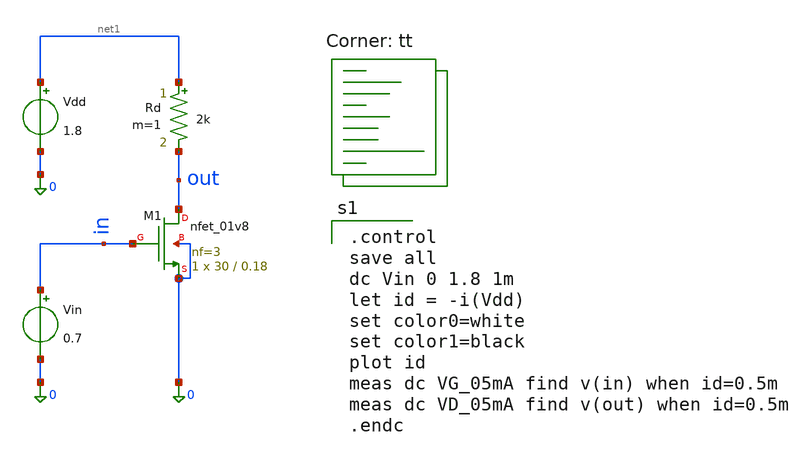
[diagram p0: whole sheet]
** sch_path: Homework 6 - Simulation on Open Source Softwares/Simulations/ex4_vgs.sch
**.subckt ex4_vgs
XM1 out in 0 0 sky130_fd_pr__nfet_01v8 L=0.18 W=30 nf=3 ad='int((3 + 1)/2) * 30 / 3 * 0.29' as='int((3 + 2)/2) * 30 / 3 * 0.29'
+ pd='2*int((3 + 1)/2) * (30 / 3 + 0.29)' ps='2*int((3 + 2)/2) * (30 / 3 + 0.29)' nrd='0.29 / 30 ' nrs='0.29 / 30 '
+ sa=0 sb=0 sd=0 mult=1 m=1
Vin in 0 0.7
Rd net1 out 2k m=1
Vdd net1 0 1.8
**** begin user architecture code
.lib $::SKYWATER_MODELS/sky130.lib.spice tt

.control
save all
dc Vin 0 1.8 1m
let id = -i(Vdd)
set color0=white
set color1=black
plot id
meas dc VG_05mA find v(in) when id=0.5m
meas dc VD_05mA find v(out) when id=0.5m
.endc

**** end user architecture code
**.ends
.end
